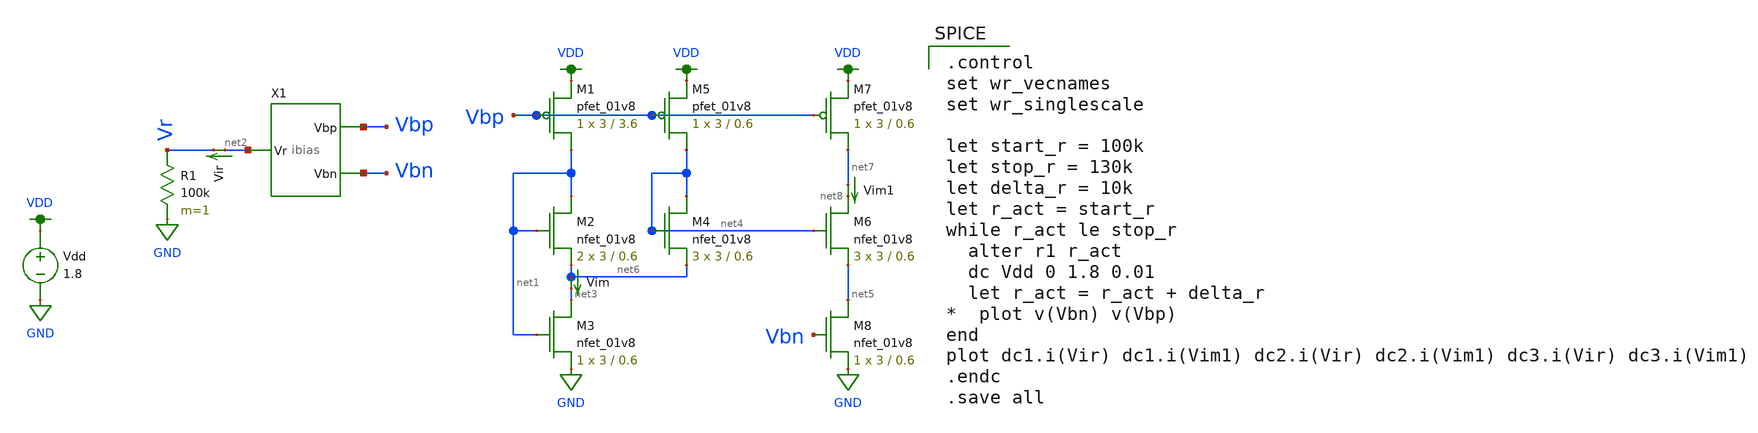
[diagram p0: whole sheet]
** sch_path: mini4/schem/ibias_test.sch
**.subckt ibias_test
Vdd VDD GND 1.8
X1 net2 Vbn Vbp ibias
R1 Vr GND 100k m=1
XM1 net1 Vbp VDD VDD sky130_fd_pr__pfet_01v8 L=3.6 W=3 nf=1 ad='int((nf+1)/2) * W/nf * 0.29' as='int((nf+2)/2) * W/nf * 0.29'
+ pd='2*int((nf+1)/2) * (W/nf + 0.29)' ps='2*int((nf+2)/2) * (W/nf + 0.29)' nrd='0.29 / W' nrs='0.29 / W'
+ sa=0 sb=0 sd=0 mult=1 m=1
XM2 net1 net1 net6 GND sky130_fd_pr__nfet_01v8 L=0.6 W=3 nf=1 ad='int((nf+1)/2) * W/nf * 0.29' as='int((nf+2)/2) * W/nf * 0.29'
+ pd='2*int((nf+1)/2) * (W/nf + 0.29)' ps='2*int((nf+2)/2) * (W/nf + 0.29)' nrd='0.29 / W' nrs='0.29 / W'
+ sa=0 sb=0 sd=0 mult=2 m=2
XM3 net3 net1 GND GND sky130_fd_pr__nfet_01v8 L=0.6 W=3 nf=1 ad='int((nf+1)/2) * W/nf * 0.29' as='int((nf+2)/2) * W/nf * 0.29'
+ pd='2*int((nf+1)/2) * (W/nf + 0.29)' ps='2*int((nf+2)/2) * (W/nf + 0.29)' nrd='0.29 / W' nrs='0.29 / W'
+ sa=0 sb=0 sd=0 mult=1 m=1
Vir net2 Vr 0
.save i(vir)
Vim net6 net3 0
.save i(vim)
XM4 net4 net4 net6 GND sky130_fd_pr__nfet_01v8 L=0.6 W=3 nf=1 ad='int((nf+1)/2) * W/nf * 0.29' as='int((nf+2)/2) * W/nf * 0.29'
+ pd='2*int((nf+1)/2) * (W/nf + 0.29)' ps='2*int((nf+2)/2) * (W/nf + 0.29)' nrd='0.29 / W' nrs='0.29 / W'
+ sa=0 sb=0 sd=0 mult=3 m=3
XM5 net4 Vbp VDD VDD sky130_fd_pr__pfet_01v8 L=0.6 W=3 nf=1 ad='int((nf+1)/2) * W/nf * 0.29' as='int((nf+2)/2) * W/nf * 0.29'
+ pd='2*int((nf+1)/2) * (W/nf + 0.29)' ps='2*int((nf+2)/2) * (W/nf + 0.29)' nrd='0.29 / W' nrs='0.29 / W'
+ sa=0 sb=0 sd=0 mult=1 m=1
XM6 net8 net4 net5 GND sky130_fd_pr__nfet_01v8 L=0.6 W=3 nf=1 ad='int((nf+1)/2) * W/nf * 0.29' as='int((nf+2)/2) * W/nf * 0.29'
+ pd='2*int((nf+1)/2) * (W/nf + 0.29)' ps='2*int((nf+2)/2) * (W/nf + 0.29)' nrd='0.29 / W' nrs='0.29 / W'
+ sa=0 sb=0 sd=0 mult=3 m=3
XM8 net5 Vbn GND GND sky130_fd_pr__nfet_01v8 L=0.6 W=3 nf=1 ad='int((nf+1)/2) * W/nf * 0.29' as='int((nf+2)/2) * W/nf * 0.29'
+ pd='2*int((nf+1)/2) * (W/nf + 0.29)' ps='2*int((nf+2)/2) * (W/nf + 0.29)' nrd='0.29 / W' nrs='0.29 / W'
+ sa=0 sb=0 sd=0 mult=1 m=1
Vim1 net7 net8 0
.save i(vim1)
XM7 net7 Vbp VDD VDD sky130_fd_pr__pfet_01v8 L=0.6 W=3 nf=1 ad='int((nf+1)/2) * W/nf * 0.29' as='int((nf+2)/2) * W/nf * 0.29'
+ pd='2*int((nf+1)/2) * (W/nf + 0.29)' ps='2*int((nf+2)/2) * (W/nf + 0.29)' nrd='0.29 / W' nrs='0.29 / W'
+ sa=0 sb=0 sd=0 mult=1 m=1
**** begin user architecture code

.option wnflag=1
.param MC_SWITCH=0.0
.lib ~/skywater/skywater-pdk/libraries/sky130_fd_pr_ngspice/latest/models/sky130.lib.spice tt


.control
set wr_vecnames
set wr_singlescale

let start_r = 100k
let stop_r = 130k
let delta_r = 10k
let r_act = start_r
while r_act le stop_r
  alter r1 r_act
  dc Vdd 0 1.8 0.01
  let r_act = r_act + delta_r
*  plot v(Vbn) v(Vbp)
end
plot dc1.i(Vir) dc1.i(Vim1) dc2.i(Vir) dc2.i(Vim1) dc3.i(Vir) dc3.i(Vim1)
.endc
.save all


**** end user architecture code
**.ends

* expanding   symbol:  /home/madvlsi/MADVLSI/mini4/schem/ibias.sym # of pins=3
** sym_path: mini4/schem/ibias.sym
** sch_path: mini4/schem/ibias.sch
.subckt ibias Vr Vbn Vbp
*.opin Vbn
*.opin Vbp
*.iopin Vr
XM1 net2 Vbp VDD VDD sky130_fd_pr__pfet_01v8 L=1.0 W=3 nf=1 ad='int((nf+1)/2) * W/nf * 0.29' as='int((nf+2)/2) * W/nf * 0.29'
+ pd='2*int((nf+1)/2) * (W/nf + 0.29)' ps='2*int((nf+2)/2) * (W/nf + 0.29)' nrd='0.29 / W' nrs='0.29 / W'
+ sa=0 sb=0 sd=0 mult=1 m=1
XM2 net1 net1 VDD VDD sky130_fd_pr__pfet_01v8 L=1.0 W=3 nf=1 ad='int((nf+1)/2) * W/nf * 0.29' as='int((nf+2)/2) * W/nf * 0.29'
+ pd='2*int((nf+1)/2) * (W/nf + 0.29)' ps='2*int((nf+2)/2) * (W/nf + 0.29)' nrd='0.29 / W' nrs='0.29 / W'
+ sa=0 sb=0 sd=0 mult=1 m=1
XM3 Vbp net1 VDD VDD sky130_fd_pr__pfet_01v8 L=1.0 W=3 nf=1 ad='int((nf+1)/2) * W/nf * 0.29' as='int((nf+2)/2) * W/nf * 0.29'
+ pd='2*int((nf+1)/2) * (W/nf + 0.29)' ps='2*int((nf+2)/2) * (W/nf + 0.29)' nrd='0.29 / W' nrs='0.29 / W'
+ sa=0 sb=0 sd=0 mult=1 m=1
XM4 Vbn Vbp VDD VDD sky130_fd_pr__pfet_01v8 L=1.0 W=3 nf=1 ad='int((nf+1)/2) * W/nf * 0.29' as='int((nf+2)/2) * W/nf * 0.29'
+ pd='2*int((nf+1)/2) * (W/nf + 0.29)' ps='2*int((nf+2)/2) * (W/nf + 0.29)' nrd='0.29 / W' nrs='0.29 / W'
+ sa=0 sb=0 sd=0 mult=1 m=1
XM5 net2 net2 Vr GND sky130_fd_pr__nfet_01v8 L=1.0 W=3 nf=1 ad='int((nf+1)/2) * W/nf * 0.29' as='int((nf+2)/2) * W/nf * 0.29'
+ pd='2*int((nf+1)/2) * (W/nf + 0.29)' ps='2*int((nf+2)/2) * (W/nf + 0.29)' nrd='0.29 / W' nrs='0.29 / W'
+ sa=0 sb=0 sd=0 mult=8 m=8
XM6 net1 net2 GND GND sky130_fd_pr__nfet_01v8 L=1.0 W=3 nf=1 ad='int((nf+1)/2) * W/nf * 0.29' as='int((nf+2)/2) * W/nf * 0.29'
+ pd='2*int((nf+1)/2) * (W/nf + 0.29)' ps='2*int((nf+2)/2) * (W/nf + 0.29)' nrd='0.29 / W' nrs='0.29 / W'
+ sa=0 sb=0 sd=0 mult=1 m=1
XM7 Vbp Vbn GND GND sky130_fd_pr__nfet_01v8 L=1.0 W=3 nf=1 ad='int((nf+1)/2) * W/nf * 0.29' as='int((nf+2)/2) * W/nf * 0.29'
+ pd='2*int((nf+1)/2) * (W/nf + 0.29)' ps='2*int((nf+2)/2) * (W/nf + 0.29)' nrd='0.29 / W' nrs='0.29 / W'
+ sa=0 sb=0 sd=0 mult=1 m=1
XM8 Vbn Vbn net3 GND sky130_fd_pr__nfet_01v8 L=1.0 W=3 nf=1 ad='int((nf+1)/2) * W/nf * 0.29' as='int((nf+2)/2) * W/nf * 0.29'
+ pd='2*int((nf+1)/2) * (W/nf + 0.29)' ps='2*int((nf+2)/2) * (W/nf + 0.29)' nrd='0.29 / W' nrs='0.29 / W'
+ sa=0 sb=0 sd=0 mult=1 m=1
Vibias net3 GND 0
.save i(vibias)
.ends

.GLOBAL GND
.GLOBAL VDD
.end
